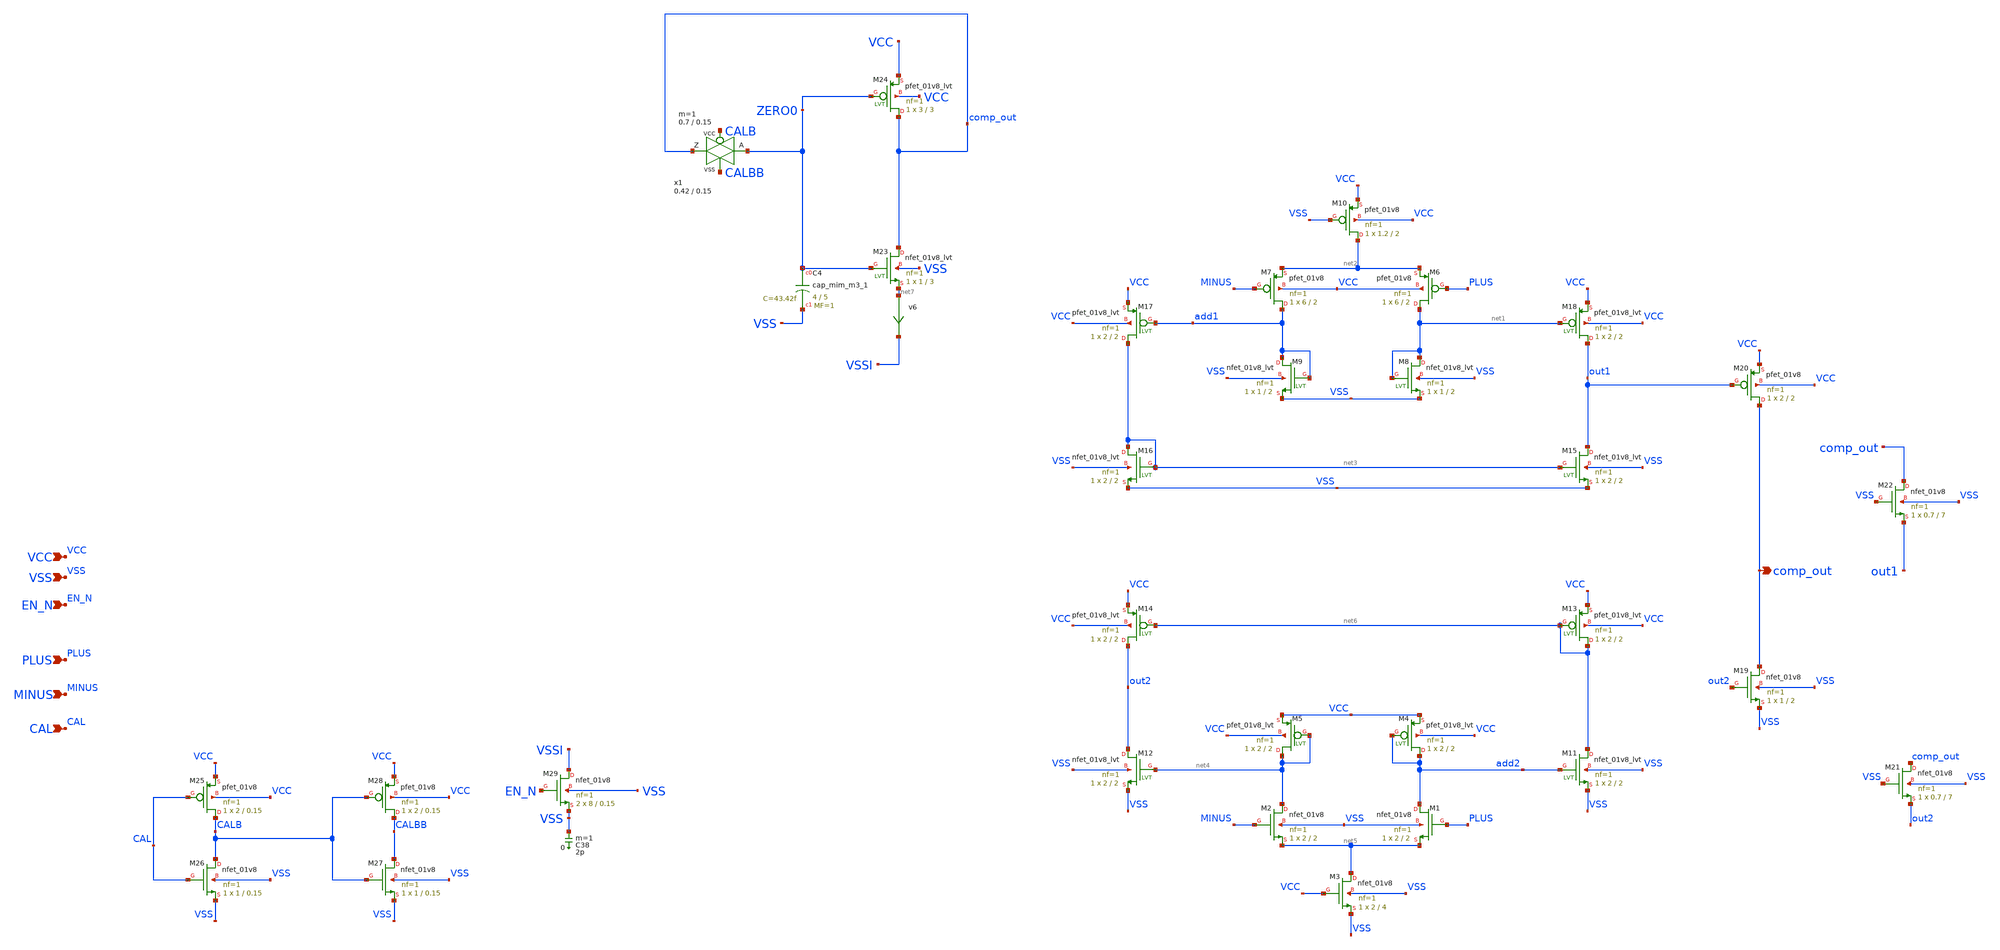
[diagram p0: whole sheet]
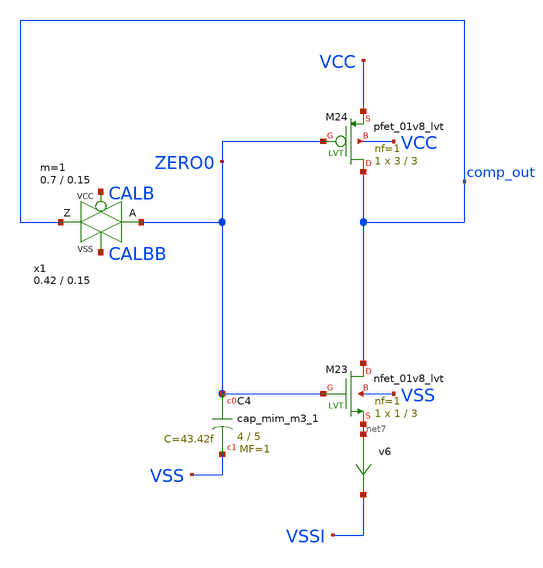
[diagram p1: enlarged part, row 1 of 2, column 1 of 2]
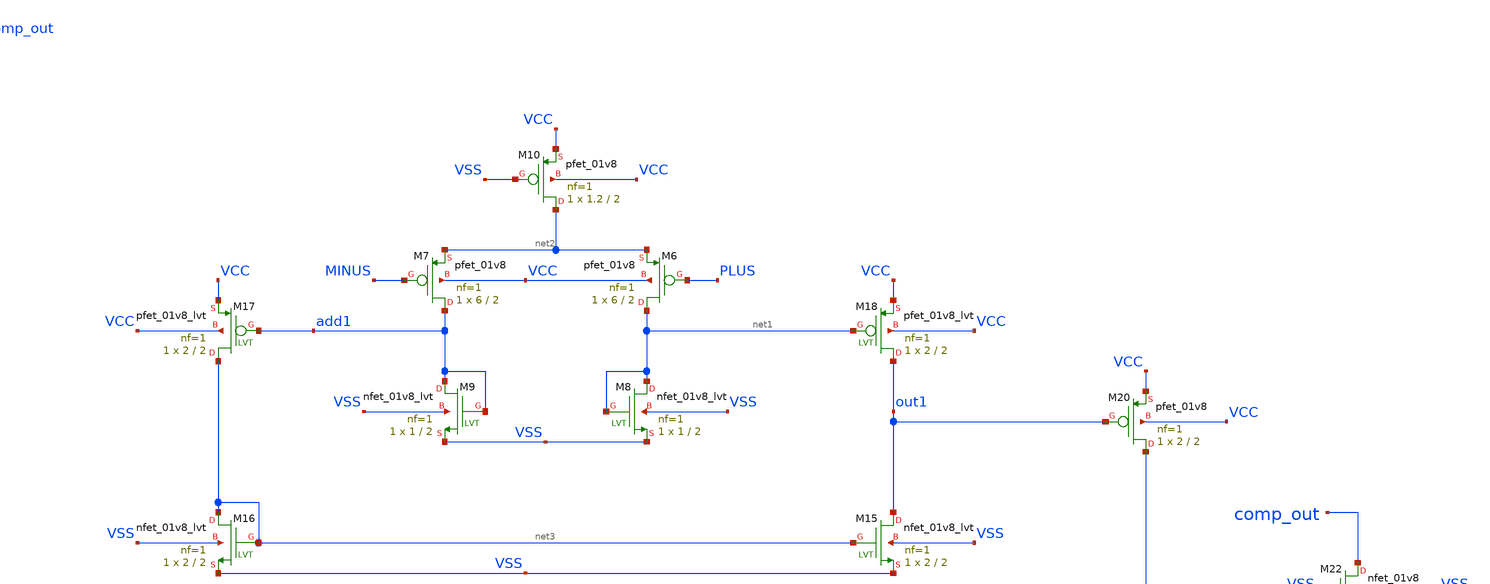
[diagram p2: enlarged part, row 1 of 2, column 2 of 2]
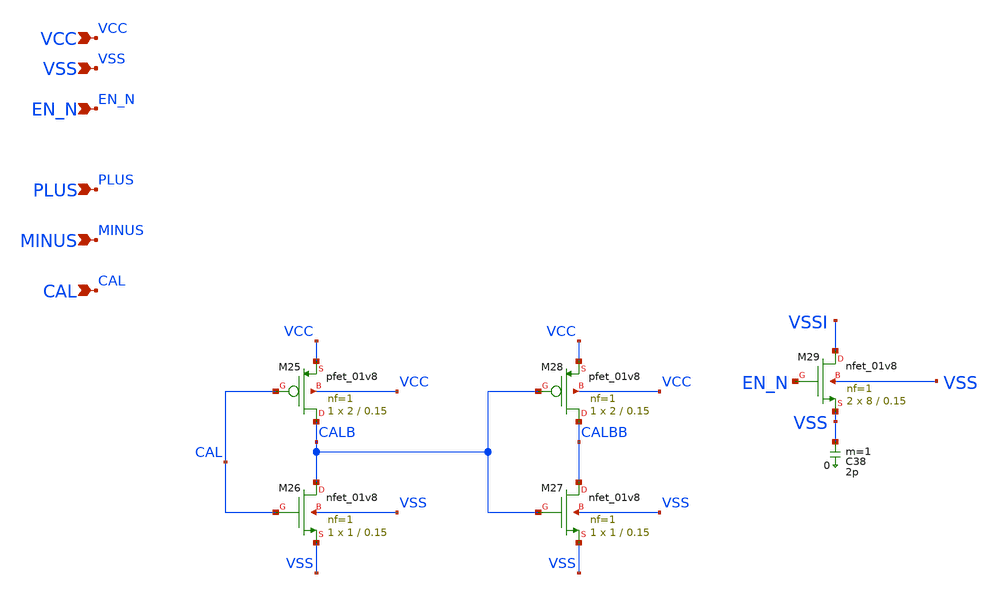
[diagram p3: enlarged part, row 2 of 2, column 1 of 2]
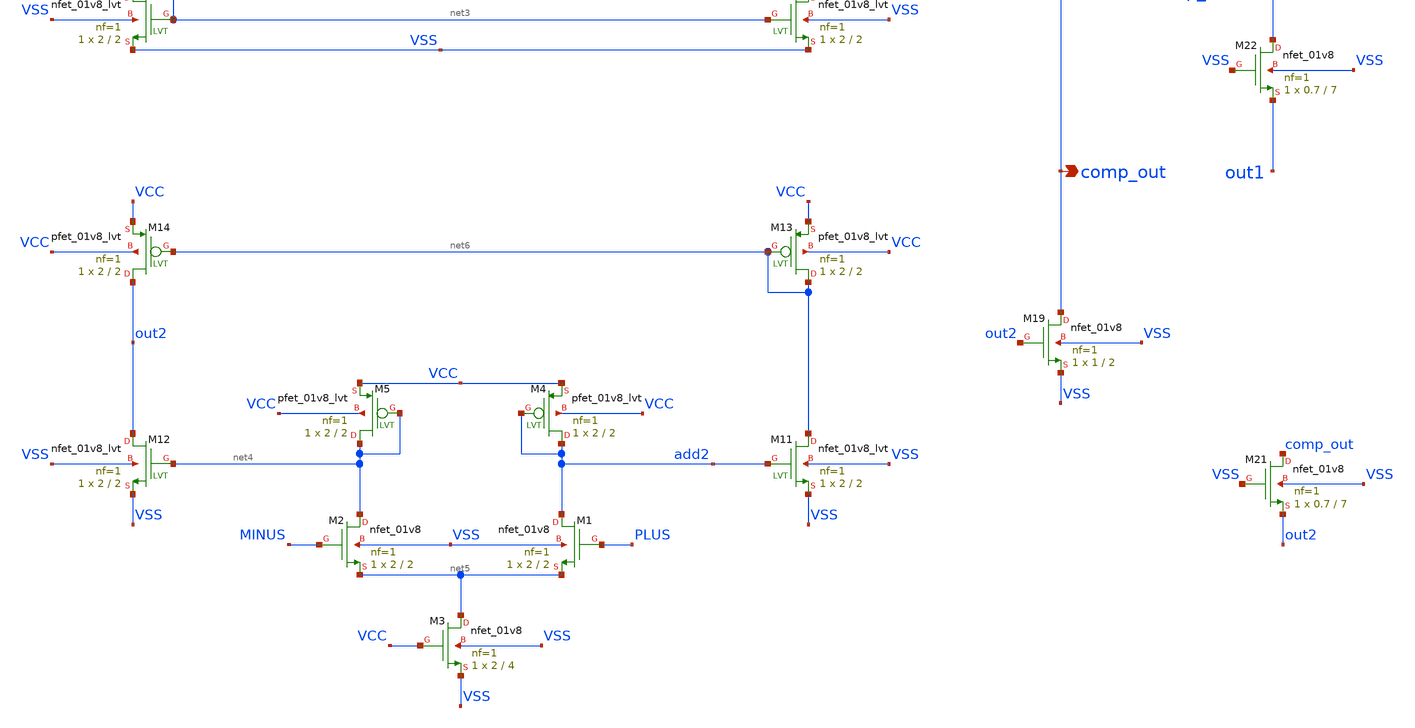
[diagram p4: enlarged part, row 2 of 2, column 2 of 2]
** sch_path: xschem/comparator.sch
**.subckt comparator VCC VSS EN_N PLUS MINUS comp_out CAL
*.ipin VCC
*.ipin VSS
*.ipin EN_N
*.ipin PLUS
*.ipin MINUS
*.opin comp_out
*.ipin CAL
v6 net7 VSSI 0
.save i(v6)
x1 comp_out ZERO0 CALB CALBB VCC VSS passgate W_N=0.42 L_N=0.15 W_P=0.7 L_P=0.15 m=1
XC4 ZERO0 VSS sky130_fd_pr__cap_mim_m3_1 W=4 L=5 MF=1 m=1
C38 VSS 0 2p m=1
XM1 add2 PLUS net5 VSS sky130_fd_pr__nfet_01v8 L=2 W=2 nf=1 ad='int((nf+1)/2) * W/nf * 0.29' as='int((nf+2)/2) * W/nf * 0.29'
+ pd='2*int((nf+1)/2) * (W/nf + 0.29)' ps='2*int((nf+2)/2) * (W/nf + 0.29)' nrd='0.29 / W' nrs='0.29 / W'
+ sa=0 sb=0 sd=0 mult=1 m=1
XM2 net4 MINUS net5 VSS sky130_fd_pr__nfet_01v8 L=2 W=2 nf=1 ad='int((nf+1)/2) * W/nf * 0.29' as='int((nf+2)/2) * W/nf * 0.29'
+ pd='2*int((nf+1)/2) * (W/nf + 0.29)' ps='2*int((nf+2)/2) * (W/nf + 0.29)' nrd='0.29 / W' nrs='0.29 / W'
+ sa=0 sb=0 sd=0 mult=1 m=1
XM3 net5 VCC VSS VSS sky130_fd_pr__nfet_01v8 L=4 W=2 nf=1 ad='int((nf+1)/2) * W/nf * 0.29' as='int((nf+2)/2) * W/nf * 0.29'
+ pd='2*int((nf+1)/2) * (W/nf + 0.29)' ps='2*int((nf+2)/2) * (W/nf + 0.29)' nrd='0.29 / W' nrs='0.29 / W'
+ sa=0 sb=0 sd=0 mult=1 m=1
XM4 add2 add2 VCC VCC sky130_fd_pr__pfet_01v8_lvt L=2 W=2 nf=1 ad='int((nf+1)/2) * W/nf * 0.29' as='int((nf+2)/2) * W/nf * 0.29'
+ pd='2*int((nf+1)/2) * (W/nf + 0.29)' ps='2*int((nf+2)/2) * (W/nf + 0.29)' nrd='0.29 / W' nrs='0.29 / W'
+ sa=0 sb=0 sd=0 mult=1 m=1
XM5 net4 net4 VCC VCC sky130_fd_pr__pfet_01v8_lvt L=2 W=2 nf=1 ad='int((nf+1)/2) * W/nf * 0.29' as='int((nf+2)/2) * W/nf * 0.29'
+ pd='2*int((nf+1)/2) * (W/nf + 0.29)' ps='2*int((nf+2)/2) * (W/nf + 0.29)' nrd='0.29 / W' nrs='0.29 / W'
+ sa=0 sb=0 sd=0 mult=1 m=1
XM6 net1 PLUS net2 VCC sky130_fd_pr__pfet_01v8 L=2 W=6 nf=1 ad='int((nf+1)/2) * W/nf * 0.29' as='int((nf+2)/2) * W/nf * 0.29'
+ pd='2*int((nf+1)/2) * (W/nf + 0.29)' ps='2*int((nf+2)/2) * (W/nf + 0.29)' nrd='0.29 / W' nrs='0.29 / W'
+ sa=0 sb=0 sd=0 mult=1 m=1
XM7 add1 MINUS net2 VCC sky130_fd_pr__pfet_01v8 L=2 W=6 nf=1 ad='int((nf+1)/2) * W/nf * 0.29' as='int((nf+2)/2) * W/nf * 0.29'
+ pd='2*int((nf+1)/2) * (W/nf + 0.29)' ps='2*int((nf+2)/2) * (W/nf + 0.29)' nrd='0.29 / W' nrs='0.29 / W'
+ sa=0 sb=0 sd=0 mult=1 m=1
XM8 net1 net1 VSS VSS sky130_fd_pr__nfet_01v8_lvt L=2 W=1 nf=1 ad='int((nf+1)/2) * W/nf * 0.29' as='int((nf+2)/2) * W/nf * 0.29'
+ pd='2*int((nf+1)/2) * (W/nf + 0.29)' ps='2*int((nf+2)/2) * (W/nf + 0.29)' nrd='0.29 / W' nrs='0.29 / W'
+ sa=0 sb=0 sd=0 mult=1 m=1
XM9 add1 add1 VSS VSS sky130_fd_pr__nfet_01v8_lvt L=2 W=1 nf=1 ad='int((nf+1)/2) * W/nf * 0.29' as='int((nf+2)/2) * W/nf * 0.29'
+ pd='2*int((nf+1)/2) * (W/nf + 0.29)' ps='2*int((nf+2)/2) * (W/nf + 0.29)' nrd='0.29 / W' nrs='0.29 / W'
+ sa=0 sb=0 sd=0 mult=1 m=1
XM10 net2 VSS VCC VCC sky130_fd_pr__pfet_01v8 L=2 W=1.2 nf=1 ad='int((nf+1)/2) * W/nf * 0.29' as='int((nf+2)/2) * W/nf * 0.29'
+ pd='2*int((nf+1)/2) * (W/nf + 0.29)' ps='2*int((nf+2)/2) * (W/nf + 0.29)' nrd='0.29 / W' nrs='0.29 / W'
+ sa=0 sb=0 sd=0 mult=1 m=1
XM14 out2 net6 VCC VCC sky130_fd_pr__pfet_01v8_lvt L=2 W=2 nf=1 ad='int((nf+1)/2) * W/nf * 0.29' as='int((nf+2)/2) * W/nf * 0.29'
+ pd='2*int((nf+1)/2) * (W/nf + 0.29)' ps='2*int((nf+2)/2) * (W/nf + 0.29)' nrd='0.29 / W' nrs='0.29 / W'
+ sa=0 sb=0 sd=0 mult=1 m=1
XM11 net6 add2 VSS VSS sky130_fd_pr__nfet_01v8_lvt L=2 W=2 nf=1 ad='int((nf+1)/2) * W/nf * 0.29' as='int((nf+2)/2) * W/nf * 0.29'
+ pd='2*int((nf+1)/2) * (W/nf + 0.29)' ps='2*int((nf+2)/2) * (W/nf + 0.29)' nrd='0.29 / W' nrs='0.29 / W'
+ sa=0 sb=0 sd=0 mult=1 m=1
XM12 out2 net4 VSS VSS sky130_fd_pr__nfet_01v8_lvt L=2 W=2 nf=1 ad='int((nf+1)/2) * W/nf * 0.29' as='int((nf+2)/2) * W/nf * 0.29'
+ pd='2*int((nf+1)/2) * (W/nf + 0.29)' ps='2*int((nf+2)/2) * (W/nf + 0.29)' nrd='0.29 / W' nrs='0.29 / W'
+ sa=0 sb=0 sd=0 mult=1 m=1
XM13 net6 net6 VCC VCC sky130_fd_pr__pfet_01v8_lvt L=2 W=2 nf=1 ad='int((nf+1)/2) * W/nf * 0.29' as='int((nf+2)/2) * W/nf * 0.29'
+ pd='2*int((nf+1)/2) * (W/nf + 0.29)' ps='2*int((nf+2)/2) * (W/nf + 0.29)' nrd='0.29 / W' nrs='0.29 / W'
+ sa=0 sb=0 sd=0 mult=1 m=1
XM15 out1 net3 VSS VSS sky130_fd_pr__nfet_01v8_lvt L=2 W=2 nf=1 ad='int((nf+1)/2) * W/nf * 0.29' as='int((nf+2)/2) * W/nf * 0.29'
+ pd='2*int((nf+1)/2) * (W/nf + 0.29)' ps='2*int((nf+2)/2) * (W/nf + 0.29)' nrd='0.29 / W' nrs='0.29 / W'
+ sa=0 sb=0 sd=0 mult=1 m=1
XM16 net3 net3 VSS VSS sky130_fd_pr__nfet_01v8_lvt L=2 W=2 nf=1 ad='int((nf+1)/2) * W/nf * 0.29' as='int((nf+2)/2) * W/nf * 0.29'
+ pd='2*int((nf+1)/2) * (W/nf + 0.29)' ps='2*int((nf+2)/2) * (W/nf + 0.29)' nrd='0.29 / W' nrs='0.29 / W'
+ sa=0 sb=0 sd=0 mult=1 m=1
XM17 net3 add1 VCC VCC sky130_fd_pr__pfet_01v8_lvt L=2 W=2 nf=1 ad='int((nf+1)/2) * W/nf * 0.29' as='int((nf+2)/2) * W/nf * 0.29'
+ pd='2*int((nf+1)/2) * (W/nf + 0.29)' ps='2*int((nf+2)/2) * (W/nf + 0.29)' nrd='0.29 / W' nrs='0.29 / W'
+ sa=0 sb=0 sd=0 mult=1 m=1
XM18 out1 net1 VCC VCC sky130_fd_pr__pfet_01v8_lvt L=2 W=2 nf=1 ad='int((nf+1)/2) * W/nf * 0.29' as='int((nf+2)/2) * W/nf * 0.29'
+ pd='2*int((nf+1)/2) * (W/nf + 0.29)' ps='2*int((nf+2)/2) * (W/nf + 0.29)' nrd='0.29 / W' nrs='0.29 / W'
+ sa=0 sb=0 sd=0 mult=1 m=1
XM19 comp_out out2 VSS VSS sky130_fd_pr__nfet_01v8 L=2 W=1 nf=1 ad='int((nf+1)/2) * W/nf * 0.29' as='int((nf+2)/2) * W/nf * 0.29'
+ pd='2*int((nf+1)/2) * (W/nf + 0.29)' ps='2*int((nf+2)/2) * (W/nf + 0.29)' nrd='0.29 / W' nrs='0.29 / W'
+ sa=0 sb=0 sd=0 mult=1 m=1
XM20 comp_out out1 VCC VCC sky130_fd_pr__pfet_01v8 L=2 W=2 nf=1 ad='int((nf+1)/2) * W/nf * 0.29' as='int((nf+2)/2) * W/nf * 0.29'
+ pd='2*int((nf+1)/2) * (W/nf + 0.29)' ps='2*int((nf+2)/2) * (W/nf + 0.29)' nrd='0.29 / W' nrs='0.29 / W'
+ sa=0 sb=0 sd=0 mult=1 m=1
XM21 comp_out VSS out2 VSS sky130_fd_pr__nfet_01v8 L=7 W=0.7 nf=1 ad='int((nf+1)/2) * W/nf * 0.29' as='int((nf+2)/2) * W/nf * 0.29'
+ pd='2*int((nf+1)/2) * (W/nf + 0.29)' ps='2*int((nf+2)/2) * (W/nf + 0.29)' nrd='0.29 / W' nrs='0.29 / W'
+ sa=0 sb=0 sd=0 mult=1 m=1
XM23 comp_out ZERO0 net7 VSS sky130_fd_pr__nfet_01v8_lvt L=3 W=1 nf=1 ad='W * 0.29' as='W * 0.29' pd='2*(W + 0.29)'
+ ps='2*(W + 0.29)' nrd=0 nrs=0 sa=0 sb=0 sd=0 mult=1 m=1
XM24 comp_out ZERO0 VCC VCC sky130_fd_pr__pfet_01v8_lvt L=3 W=3 nf=1 ad='W * 0.29' as='W * 0.29' pd='2*(W + 0.29)'
+ ps='2*(W + 0.29)' nrd=0 nrs=0 sa=0 sb=0 sd=0 mult=1 m=1
XM25 CALB CAL VCC VCC sky130_fd_pr__pfet_01v8 L=0.15 W=2 nf=1 ad='int((nf+1)/2) * W/nf * 0.29' as='int((nf+2)/2) * W/nf * 0.29'
+ pd='2*int((nf+1)/2) * (W/nf + 0.29)' ps='2*int((nf+2)/2) * (W/nf + 0.29)' nrd='0.29 / W' nrs='0.29 / W'
+ sa=0 sb=0 sd=0 mult=1 m=1
XM26 CALB CAL VSS VSS sky130_fd_pr__nfet_01v8 L=0.15 W=1 nf=1 ad='int((nf+1)/2) * W/nf * 0.29' as='int((nf+2)/2) * W/nf * 0.29'
+ pd='2*int((nf+1)/2) * (W/nf + 0.29)' ps='2*int((nf+2)/2) * (W/nf + 0.29)' nrd='0.29 / W' nrs='0.29 / W'
+ sa=0 sb=0 sd=0 mult=1 m=1
XM27 CALBB CALB VSS VSS sky130_fd_pr__nfet_01v8 L=0.15 W=1 nf=1 ad='int((nf+1)/2) * W/nf * 0.29' as='int((nf+2)/2) * W/nf * 0.29'
+ pd='2*int((nf+1)/2) * (W/nf + 0.29)' ps='2*int((nf+2)/2) * (W/nf + 0.29)' nrd='0.29 / W' nrs='0.29 / W'
+ sa=0 sb=0 sd=0 mult=1 m=1
XM28 CALBB CALB VCC VCC sky130_fd_pr__pfet_01v8 L=0.15 W=2 nf=1 ad='int((nf+1)/2) * W/nf * 0.29' as='int((nf+2)/2) * W/nf * 0.29'
+ pd='2*int((nf+1)/2) * (W/nf + 0.29)' ps='2*int((nf+2)/2) * (W/nf + 0.29)' nrd='0.29 / W' nrs='0.29 / W'
+ sa=0 sb=0 sd=0 mult=1 m=1
XM29 VSSI EN_N VSS VSS sky130_fd_pr__nfet_01v8 L=0.15 W=8 nf=1 ad='W * 0.29' as='W * 0.29' pd='W + 2 * 0.29'
+ ps='W + 2 * 0.29' nrd=0 nrs=0 sa=0 sb=0 sd=0 mult=2 m=2
XM22 comp_out VSS out1 VSS sky130_fd_pr__nfet_01v8 L=7 W=0.7 nf=1 ad='int((nf+1)/2) * W/nf * 0.29' as='int((nf+2)/2) * W/nf * 0.29'
+ pd='2*int((nf+1)/2) * (W/nf + 0.29)' ps='2*int((nf+2)/2) * (W/nf + 0.29)' nrd='0.29 / W' nrs='0.29 / W'
+ sa=0 sb=0 sd=0 mult=1 m=1
**.ends

* expanding   symbol:  sky130_tests/passgate.sym # of pins=4
** sym_path: sky130_tests/passgate.sym
** sch_path: sky130_tests/passgate.sch
.subckt passgate Z A GP GN VCCBPIN VSSBPIN  W_N=1 L_N=0.2 W_P=1 L_P=0.2

*.iopin A
*.iopin Z
*.ipin GP
*.ipin GN
XM1 A GN Z VSS sky130_fd_pr__nfet_01v8 W=W_N L=L_N ad='W * 0.29' pd='W + 2 * 0.29' as='W * 0.29' ps='W + 2 * 0.29'
+ nrd=0 nrs=0 sa=0 sb=0 sd=0 nf=1 mult=1
XM2 A GP Z VCC sky130_fd_pr__pfet_01v8 W=W_P L=L_P ad='W * 0.29' pd='W + 2 * 0.29' as='W * 0.29' ps='W + 2 * 0.29'
+ nrd=0 nrs=0 sa=0 sb=0 sd=0 nf=1 mult=1
.ends

.end
